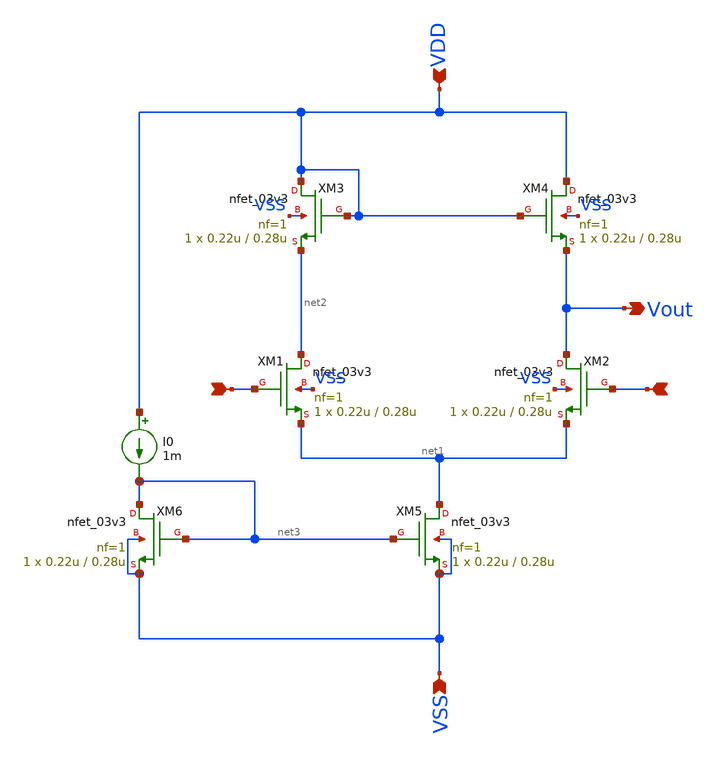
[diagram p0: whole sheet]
** sch_path: xschem/ota_miller/ota_n_in.sch
**.subckt ota_n_in Vout VSS VDD + -
*.opin Vout
*.ipin VSS
*.ipin VDD
*.ipin +
*.ipin -
XM1 net2 + net1 VSS nfet_03v3 L=0.28u W=0.22u nf=1 ad='int((nf+1)/2) * W/nf * 0.18u' as='int((nf+2)/2) * W/nf * 0.18u'
+ pd='2*int((nf+1)/2) * (W/nf + 0.18u)' ps='2*int((nf+2)/2) * (W/nf + 0.18u)' nrd='0.18u / W' nrs='0.18u / W'
+ sa=0 sb=0 sd=0 m=1 par=1
XM2 Vout - net1 VSS nfet_03v3 L=0.28u W=0.22u nf=1 ad='int((nf+1)/2) * W/nf * 0.18u' as='int((nf+2)/2) * W/nf * 0.18u'
+ pd='2*int((nf+1)/2) * (W/nf + 0.18u)' ps='2*int((nf+2)/2) * (W/nf + 0.18u)' nrd='0.18u / W' nrs='0.18u / W'
+ sa=0 sb=0 sd=0 m=1 par=1
XM3 VDD VDD net2 VSS nfet_03v3 L=0.28u W=0.22u nf=1 ad='int((nf+1)/2) * W/nf * 0.18u' as='int((nf+2)/2) * W/nf * 0.18u'
+ pd='2*int((nf+1)/2) * (W/nf + 0.18u)' ps='2*int((nf+2)/2) * (W/nf + 0.18u)' nrd='0.18u / W' nrs='0.18u / W'
+ sa=0 sb=0 sd=0 m=1 par=1
XM4 VDD VDD Vout VSS nfet_03v3 L=0.28u W=0.22u nf=1 ad='int((nf+1)/2) * W/nf * 0.18u' as='int((nf+2)/2) * W/nf * 0.18u'
+ pd='2*int((nf+1)/2) * (W/nf + 0.18u)' ps='2*int((nf+2)/2) * (W/nf + 0.18u)' nrd='0.18u / W' nrs='0.18u / W'
+ sa=0 sb=0 sd=0 m=1 par=1
XM5 net1 net3 VSS VSS nfet_03v3 L=0.28u W=0.22u nf=1 ad='int((nf+1)/2) * W/nf * 0.18u' as='int((nf+2)/2) * W/nf * 0.18u'
+ pd='2*int((nf+1)/2) * (W/nf + 0.18u)' ps='2*int((nf+2)/2) * (W/nf + 0.18u)' nrd='0.18u / W' nrs='0.18u / W'
+ sa=0 sb=0 sd=0 m=1 par=1
XM6 net3 net3 VSS VSS nfet_03v3 L=0.28u W=0.22u nf=1 ad='int((nf+1)/2) * W/nf * 0.18u' as='int((nf+2)/2) * W/nf * 0.18u'
+ pd='2*int((nf+1)/2) * (W/nf + 0.18u)' ps='2*int((nf+2)/2) * (W/nf + 0.18u)' nrd='0.18u / W' nrs='0.18u / W'
+ sa=0 sb=0 sd=0 m=1 par=1
I0 VDD net3 1m
**.ends
.end
